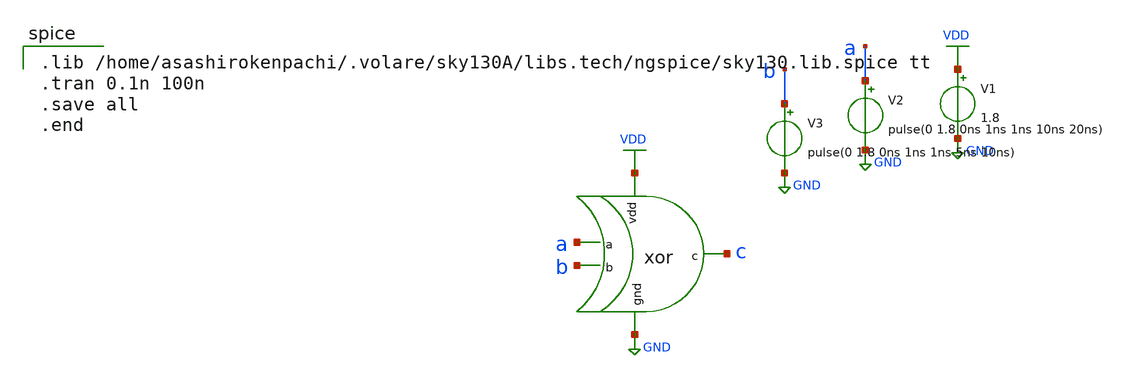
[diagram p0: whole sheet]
** sch_path: xor_post_sym_sim.sch
**.subckt xor_post_sym_sim
x1 VDD GND a b c xor
V1 VDD GND 1.8
V2 a GND pulse(0 1.8 0ns 1ns 1ns 10ns 20ns)
V3 b GND pulse(0 1.8 0ns 1ns 1ns 5ns 10ns)
**** begin user architecture code

.lib /home/asashirokenpachi/.volare/sky130A/libs.tech/ngspice/sky130.lib.spice tt
.tran 0.1n 100n
.save all
.end

**** end user architecture code
**.ends
.GLOBAL GND
.GLOBAL VDD
.end
